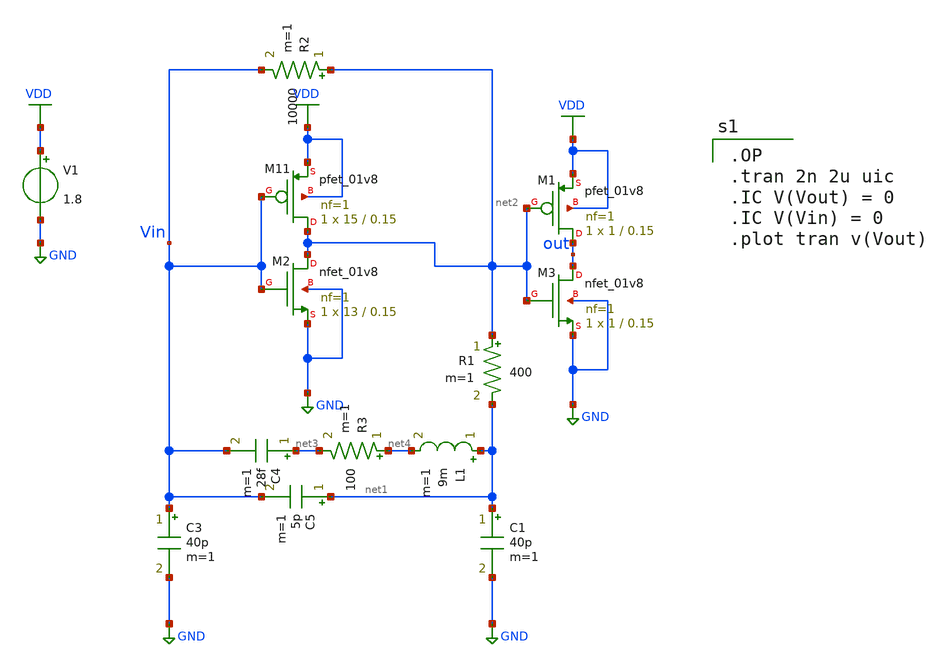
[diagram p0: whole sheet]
** sch_path: pll/xctl_lib_V2/xctl/xschem/Crystal.sch
**.subckt Crystal
R1 net2 net1 400 m=1
R2 net2 Vin 10000 m=1
C1 net1 GND 40p m=1
C3 Vin GND 40p m=1
V1 VDD GND 1.8
L1 net1 net4 9m m=1
R3 net4 net3 100 m=1
C4 net3 Vin 28f m=1
C5 net1 Vin 5p m=1
XM11 net2 Vin VDD VDD sky130_fd_pr__pfet_01v8 L=0.15 W=15 nf=1 ad='int((nf+1)/2) * W/nf * 0.29' as='int((nf+2)/2) * W/nf * 0.29'
+ pd='2*int((nf+1)/2) * (W/nf + 0.29)' ps='2*int((nf+2)/2) * (W/nf + 0.29)' nrd='0.29 / W' nrs='0.29 / W'
+ sa=0 sb=0 sd=0 mult=1 m=1
XM2 net2 Vin GND GND sky130_fd_pr__nfet_01v8 L=0.15 W=13 nf=1 ad='int((1 + 1)/2) * 13 / 1 * 0.29' as='int((1 + 2)/2) * 13 / 1 * 0.29'
+ pd='2*int((1 + 1)/2) * (13 / 1 + 0.29)' ps='2*int((1 + 2)/2) * (13 / 1 + 0.29)' nrd='0.29 / 13 ' nrs='0.29 / 13 '
+ sa=0 sb=0 sd=0 mult=1 m=1
XM1 out net2 VDD VDD sky130_fd_pr__pfet_01v8 L=0.15 W=1 nf=1 ad='int((nf+1)/2) * W/nf * 0.29' as='int((nf+2)/2) * W/nf * 0.29'
+ pd='2*int((nf+1)/2) * (W/nf + 0.29)' ps='2*int((nf+2)/2) * (W/nf + 0.29)' nrd='0.29 / W' nrs='0.29 / W'
+ sa=0 sb=0 sd=0 mult=1 m=1
XM3 out net2 GND GND sky130_fd_pr__nfet_01v8 L=0.15 W=1 nf=1 ad='int((1 + 1)/2) * 1 / 1 * 0.29' as='int((1 + 2)/2) * 1 / 1 * 0.29'
+ pd='2*int((1 + 1)/2) * (1 / 1 + 0.29)' ps='2*int((1 + 2)/2) * (1 / 1 + 0.29)' nrd='0.29 / 1 ' nrs='0.29 / 1 '
+ sa=0 sb=0 sd=0 mult=1 m=1
**** begin user architecture code

** opencircuitdesign pdks install
.lib $::SKYWATER_MODELS/sky130.lib.spice tt



.OP
.tran 2n 2u uic
.IC V(Vout) = 0
.IC V(Vin) = 0
.plot tran v(Vout)


**** end user architecture code
**.ends
.GLOBAL GND
.GLOBAL VDD
.end
